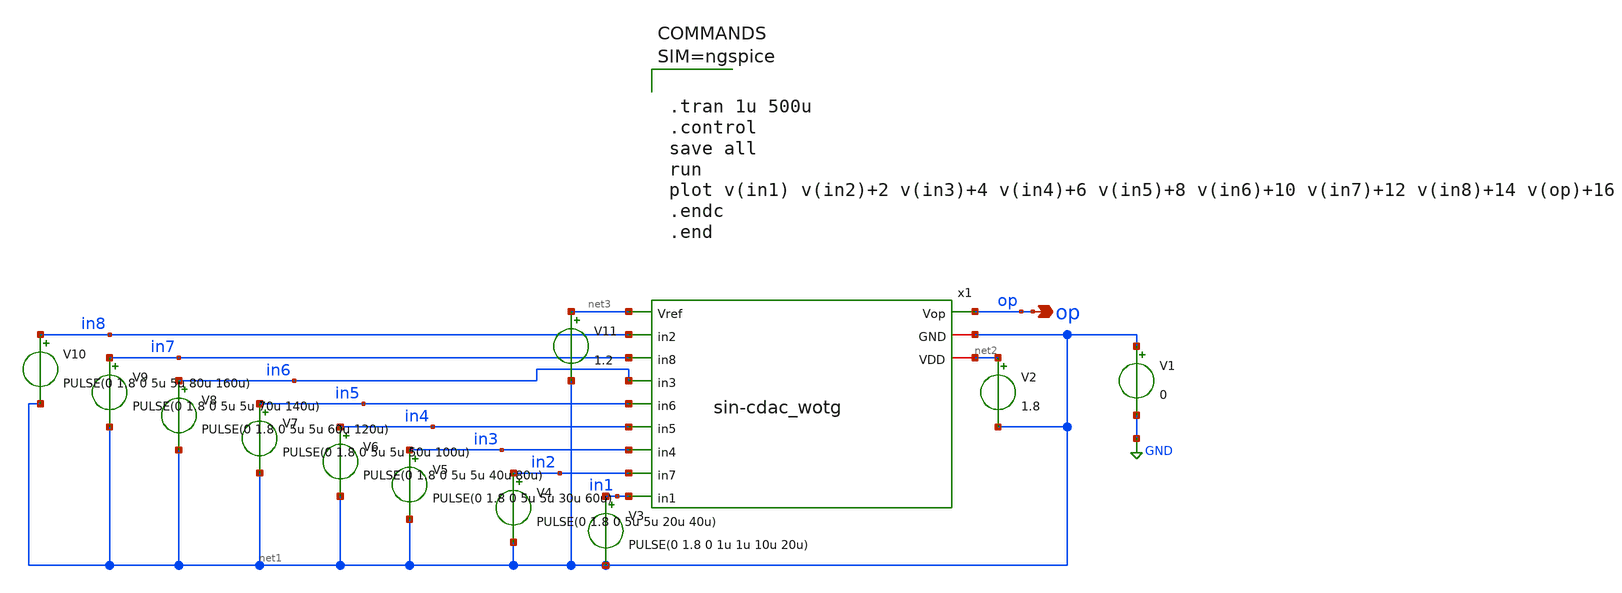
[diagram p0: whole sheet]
** sch_path: sar-adc/updated/tb-wotg-cdac.sch
**.subckt tb-wotg-cdac op
*.opin op
x1 op net1 net3 in8 in7 in6 in5 in4 in3 in2 in1 net2 sin-cdac_wotg
V1 net1 GND 0
V2 net2 net1 1.8
V3 in1 net1 PULSE(0 1.8 0 1u 1u 10u 20u)
V4 in2 net1 PULSE(0 1.8 0 5u 5u 20u 40u)
V5 in3 net1 PULSE(0 1.8 0 5u 5u 30u 60u)
V6 in4 net1 PULSE(0 1.8 0 5u 5u 40u 80u)
V7 in5 net1 PULSE(0 1.8 0 5u 5u 50u 100u)
V8 in6 net1 PULSE(0 1.8 0 5u 5u 60u 120u)
V9 in7 net1 PULSE(0 1.8 0 5u 5u 70u 140u)
V10 in8 net1 PULSE(0 1.8 0 5u 5u 80u 160u)
V11 net3 net1 1.2
**** begin user architecture code

** opencircuitdesign pdks install
.lib $::SKYWATER_MODELS/sky130.lib.spice tt




.tran 1u 500u
.control
save all
run
plot v(in1) v(in2)+2 v(in3)+4 v(in4)+6 v(in5)+8 v(in6)+10 v(in7)+12 v(in8)+14 v(op)+16
.endc
.end



**** end user architecture code
**.ends

* expanding   symbol:  sin-cdac_wotg.sym # of pins=12
** sym_path: sar-adc/updated/sin-cdac_wotg.sym
** sch_path: sar-adc/updated/sin-cdac_wotg.sch
.subckt sin-cdac_wotg Vop GND Vref in2 in8 in3 in6 in5 in4 in7 in1 VDD
*.ipin Vref
*.iopin VDD
*.opin Vop
*.iopin GND
*.ipin in1
*.ipin in2
*.ipin in3
*.ipin in4
*.ipin in5
*.ipin in6
*.ipin in7
*.ipin in8
XC1 Vop net1 sky130_fd_pr__cap_mim_m3_1 W=1 L=1 MF=128 m=128
XC3 Vop net2 sky130_fd_pr__cap_mim_m3_1 W=1 L=1 MF=64 m=64
XC4 Vop net2 sky130_fd_pr__cap_mim_m3_1 W=1 L=1 MF=64 m=64
XC5 Vop net3 sky130_fd_pr__cap_mim_m3_1 W=1 L=1 MF=32 m=32
XC6 Vop net3 sky130_fd_pr__cap_mim_m3_1 W=1 L=1 MF=32 m=32
XC7 Vop net4 sky130_fd_pr__cap_mim_m3_1 W=1 L=1 MF=16 m=16
XC8 Vop net4 sky130_fd_pr__cap_mim_m3_1 W=1 L=1 MF=16 m=16
XC9 Vop net5 sky130_fd_pr__cap_mim_m3_1 W=1 L=1 MF=8 m=8
XC10 Vop net5 sky130_fd_pr__cap_mim_m3_1 W=1 L=1 MF=8 m=8
XC11 Vop net6 sky130_fd_pr__cap_mim_m3_1 W=1 L=1 MF=4 m=4
XC12 Vop net6 sky130_fd_pr__cap_mim_m3_1 W=1 L=1 MF=4 m=4
XC13 Vop net7 sky130_fd_pr__cap_mim_m3_1 W=1 L=1 MF=2 m=2
XC14 Vop net7 sky130_fd_pr__cap_mim_m3_1 W=1 L=1 MF=2 m=2
XC15 Vop net8 sky130_fd_pr__cap_mim_m3_1 W=1 L=1 MF=1 m=1
XC16 Vop net8 sky130_fd_pr__cap_mim_m3_1 W=1 L=1 MF=1 m=1
XM2 net1 in1 GND GND sky130_fd_pr__nfet_01v8 L=0.15 W=1 nf=1 ad='int((1 + 1)/2) * 1 / 1 * 0.29' as='int((1 + 2)/2) * 1 / 1 * 0.29'
+ pd='2*int((1 + 1)/2) * (1 / 1 + 0.29)' ps='2*int((1 + 2)/2) * (1 / 1 + 0.29)' nrd='0.29 / 1 ' nrs='0.29 / 1 '
+ sa=0 sb=0 sd=0 mult=1 m=1
XM1 net2 in2 GND GND sky130_fd_pr__nfet_01v8 L=0.15 W=1 nf=1 ad='int((1 + 1)/2) * 1 / 1 * 0.29' as='int((1 + 2)/2) * 1 / 1 * 0.29'
+ pd='2*int((1 + 1)/2) * (1 / 1 + 0.29)' ps='2*int((1 + 2)/2) * (1 / 1 + 0.29)' nrd='0.29 / 1 ' nrs='0.29 / 1 '
+ sa=0 sb=0 sd=0 mult=1 m=1
XM3 net3 in3 GND GND sky130_fd_pr__nfet_01v8 L=0.15 W=1 nf=1 ad='int((1 + 1)/2) * 1 / 1 * 0.29' as='int((1 + 2)/2) * 1 / 1 * 0.29'
+ pd='2*int((1 + 1)/2) * (1 / 1 + 0.29)' ps='2*int((1 + 2)/2) * (1 / 1 + 0.29)' nrd='0.29 / 1 ' nrs='0.29 / 1 '
+ sa=0 sb=0 sd=0 mult=1 m=1
XM4 net4 in4 GND GND sky130_fd_pr__nfet_01v8 L=0.15 W=1 nf=1 ad='int((1 + 1)/2) * 1 / 1 * 0.29' as='int((1 + 2)/2) * 1 / 1 * 0.29'
+ pd='2*int((1 + 1)/2) * (1 / 1 + 0.29)' ps='2*int((1 + 2)/2) * (1 / 1 + 0.29)' nrd='0.29 / 1 ' nrs='0.29 / 1 '
+ sa=0 sb=0 sd=0 mult=1 m=1
XM5 net5 in5 GND GND sky130_fd_pr__nfet_01v8 L=0.15 W=1 nf=1 ad='int((1 + 1)/2) * 1 / 1 * 0.29' as='int((1 + 2)/2) * 1 / 1 * 0.29'
+ pd='2*int((1 + 1)/2) * (1 / 1 + 0.29)' ps='2*int((1 + 2)/2) * (1 / 1 + 0.29)' nrd='0.29 / 1 ' nrs='0.29 / 1 '
+ sa=0 sb=0 sd=0 mult=1 m=1
XM6 net6 in6 GND GND sky130_fd_pr__nfet_01v8 L=0.15 W=1 nf=1 ad='int((1 + 1)/2) * 1 / 1 * 0.29' as='int((1 + 2)/2) * 1 / 1 * 0.29'
+ pd='2*int((1 + 1)/2) * (1 / 1 + 0.29)' ps='2*int((1 + 2)/2) * (1 / 1 + 0.29)' nrd='0.29 / 1 ' nrs='0.29 / 1 '
+ sa=0 sb=0 sd=0 mult=1 m=1
XM7 net7 in7 GND GND sky130_fd_pr__nfet_01v8 L=0.15 W=1 nf=1 ad='int((1 + 1)/2) * 1 / 1 * 0.29' as='int((1 + 2)/2) * 1 / 1 * 0.29'
+ pd='2*int((1 + 1)/2) * (1 / 1 + 0.29)' ps='2*int((1 + 2)/2) * (1 / 1 + 0.29)' nrd='0.29 / 1 ' nrs='0.29 / 1 '
+ sa=0 sb=0 sd=0 mult=1 m=1
XM8 net8 in8 GND GND sky130_fd_pr__nfet_01v8 L=0.15 W=1 nf=1 ad='int((1 + 1)/2) * 1 / 1 * 0.29' as='int((1 + 2)/2) * 1 / 1 * 0.29'
+ pd='2*int((1 + 1)/2) * (1 / 1 + 0.29)' ps='2*int((1 + 2)/2) * (1 / 1 + 0.29)' nrd='0.29 / 1 ' nrs='0.29 / 1 '
+ sa=0 sb=0 sd=0 mult=1 m=1
XM17 Vref in1 net1 VDD sky130_fd_pr__pfet_01v8 L=0.15 W=1 nf=1 ad='int((nf+1)/2) * W/nf * 0.29' as='int((nf+2)/2) * W/nf * 0.29'
+ pd='2*int((nf+1)/2) * (W/nf + 0.29)' ps='2*int((nf+2)/2) * (W/nf + 0.29)' nrd='0.29 / W' nrs='0.29 / W'
+ sa=0 sb=0 sd=0 mult=1 m=1
XM18 Vref in2 net2 VDD sky130_fd_pr__pfet_01v8 L=0.15 W=1 nf=1 ad='int((nf+1)/2) * W/nf * 0.29' as='int((nf+2)/2) * W/nf * 0.29'
+ pd='2*int((nf+1)/2) * (W/nf + 0.29)' ps='2*int((nf+2)/2) * (W/nf + 0.29)' nrd='0.29 / W' nrs='0.29 / W'
+ sa=0 sb=0 sd=0 mult=1 m=1
XM19 Vref in3 net3 VDD sky130_fd_pr__pfet_01v8 L=0.15 W=1 nf=1 ad='int((nf+1)/2) * W/nf * 0.29' as='int((nf+2)/2) * W/nf * 0.29'
+ pd='2*int((nf+1)/2) * (W/nf + 0.29)' ps='2*int((nf+2)/2) * (W/nf + 0.29)' nrd='0.29 / W' nrs='0.29 / W'
+ sa=0 sb=0 sd=0 mult=1 m=1
XM20 Vref in4 net4 VDD sky130_fd_pr__pfet_01v8 L=0.15 W=1 nf=1 ad='int((nf+1)/2) * W/nf * 0.29' as='int((nf+2)/2) * W/nf * 0.29'
+ pd='2*int((nf+1)/2) * (W/nf + 0.29)' ps='2*int((nf+2)/2) * (W/nf + 0.29)' nrd='0.29 / W' nrs='0.29 / W'
+ sa=0 sb=0 sd=0 mult=1 m=1
XM21 Vref in5 net5 VDD sky130_fd_pr__pfet_01v8 L=0.15 W=1 nf=1 ad='int((nf+1)/2) * W/nf * 0.29' as='int((nf+2)/2) * W/nf * 0.29'
+ pd='2*int((nf+1)/2) * (W/nf + 0.29)' ps='2*int((nf+2)/2) * (W/nf + 0.29)' nrd='0.29 / W' nrs='0.29 / W'
+ sa=0 sb=0 sd=0 mult=1 m=1
XM22 Vref in6 net6 VDD sky130_fd_pr__pfet_01v8 L=0.15 W=1 nf=1 ad='int((nf+1)/2) * W/nf * 0.29' as='int((nf+2)/2) * W/nf * 0.29'
+ pd='2*int((nf+1)/2) * (W/nf + 0.29)' ps='2*int((nf+2)/2) * (W/nf + 0.29)' nrd='0.29 / W' nrs='0.29 / W'
+ sa=0 sb=0 sd=0 mult=1 m=1
XM23 Vref in7 net7 VDD sky130_fd_pr__pfet_01v8 L=0.15 W=1 nf=1 ad='int((nf+1)/2) * W/nf * 0.29' as='int((nf+2)/2) * W/nf * 0.29'
+ pd='2*int((nf+1)/2) * (W/nf + 0.29)' ps='2*int((nf+2)/2) * (W/nf + 0.29)' nrd='0.29 / W' nrs='0.29 / W'
+ sa=0 sb=0 sd=0 mult=1 m=1
XM24 Vref in8 net8 VDD sky130_fd_pr__pfet_01v8 L=0.15 W=1 nf=1 ad='int((nf+1)/2) * W/nf * 0.29' as='int((nf+2)/2) * W/nf * 0.29'
+ pd='2*int((nf+1)/2) * (W/nf + 0.29)' ps='2*int((nf+2)/2) * (W/nf + 0.29)' nrd='0.29 / W' nrs='0.29 / W'
+ sa=0 sb=0 sd=0 mult=1 m=1
XC2 Vop net1 sky130_fd_pr__cap_mim_m3_1 W=1 L=1 MF=128 m=128
.ends

.GLOBAL GND
.end
